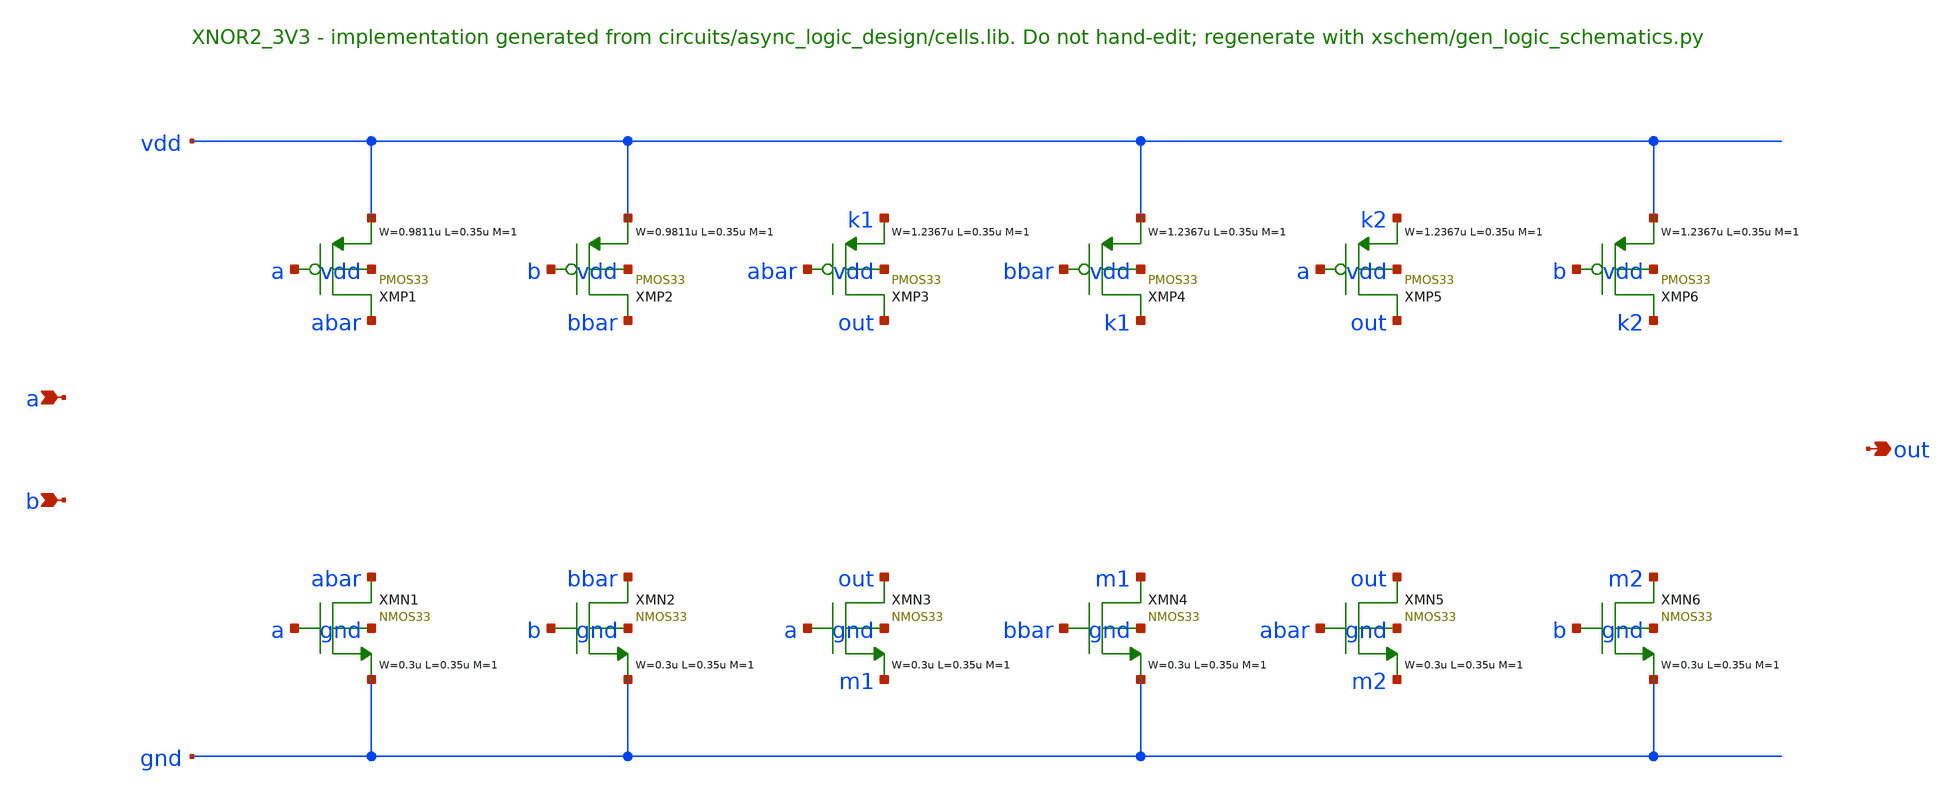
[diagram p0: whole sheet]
** sch_path: xschem/logic/XNOR2_3V3.sch
**.subckt XNOR2_3V3 a b out
*.ipin a
*.ipin b
*.opin out
XMP1 abar a vdd vdd PMOS33 W=0.9811u L=0.35u M=1 MM_SIGMA=0
XMP2 bbar b vdd vdd PMOS33 W=0.9811u L=0.35u M=1 MM_SIGMA=0
XMP3 out abar k1 vdd PMOS33 W=1.2367u L=0.35u M=1 MM_SIGMA=0
XMP4 k1 bbar vdd vdd PMOS33 W=1.2367u L=0.35u M=1 MM_SIGMA=0
XMP5 out a k2 vdd PMOS33 W=1.2367u L=0.35u M=1 MM_SIGMA=0
XMP6 k2 b vdd vdd PMOS33 W=1.2367u L=0.35u M=1 MM_SIGMA=0
XMN1 abar a gnd gnd NMOS33 W=0.3u L=0.35u M=1 MM_SIGMA=0
XMN2 bbar b gnd gnd NMOS33 W=0.3u L=0.35u M=1 MM_SIGMA=0
XMN3 out a m1 gnd NMOS33 W=0.3u L=0.35u M=1 MM_SIGMA=0
XMN4 m1 bbar gnd gnd NMOS33 W=0.3u L=0.35u M=1 MM_SIGMA=0
XMN5 out abar m2 gnd NMOS33 W=0.3u L=0.35u M=1 MM_SIGMA=0
XMN6 m2 b gnd gnd NMOS33 W=0.3u L=0.35u M=1 MM_SIGMA=0
**.ends
.end
